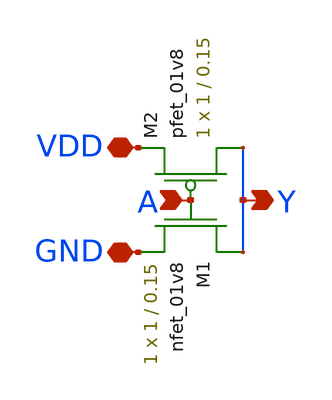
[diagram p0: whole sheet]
** sch_path: Final DAC files/schematics/Inverter/inverter.sch
**.subckt inverter A VDD GND Y
*.ipin A
*.iopin VDD
*.iopin GND
*.opin Y
XM1 Y A GND GND sky130_fd_pr__nfet_01v8 L=0.15 W=1 nf=1 ad='int((nf+1)/2) * W/nf * 0.29' as='int((nf+2)/2) * W/nf * 0.29'
+ pd='2*int((nf+1)/2) * (W/nf + 0.29)' ps='2*int((nf+2)/2) * (W/nf + 0.29)' nrd='0.29 / W' nrs='0.29 / W'
+ sa=0 sb=0 sd=0 mult=1 m=1
XM2 Y A VDD VDD sky130_fd_pr__pfet_01v8 L=0.15 W=1 nf=1 ad='int((nf+1)/2) * W/nf * 0.29' as='int((nf+2)/2) * W/nf * 0.29'
+ pd='2*int((nf+1)/2) * (W/nf + 0.29)' ps='2*int((nf+2)/2) * (W/nf + 0.29)' nrd='0.29 / W' nrs='0.29 / W'
+ sa=0 sb=0 sd=0 mult=1 m=1
**.ends
.end
